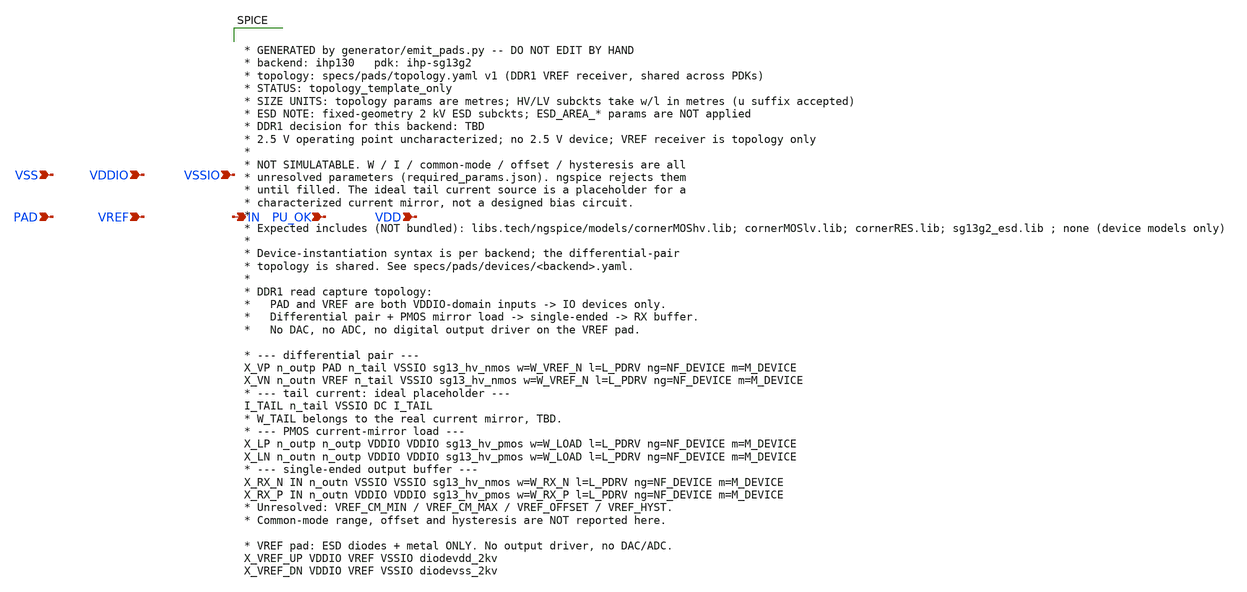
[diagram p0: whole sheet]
** sch_path: sch/pads/ihp130/vref_receiver.sch
**.subckt vref_receiver PAD VREF IN PU_OK VDD VSS VDDIO VSSIO
*.ipin PAD
*.ipin VREF
*.opin IN
*.ipin PU_OK
*.ipin VDD
*.ipin VSS
*.ipin VDDIO
*.ipin VSSIO
**** begin user architecture code


* GENERATED by generator/emit_pads.py -- DO NOT EDIT BY HAND
* backend: ihp130   pdk: ihp-sg13g2
* topology: specs/pads/topology.yaml v1 (DDR1 VREF receiver, shared across PDKs)
* STATUS: topology_template_only
* SIZE UNITS: topology params are metres; HV/LV subckts take w/l in metres (u suffix accepted)
* ESD NOTE: fixed-geometry 2 kV ESD subckts; ESD_AREA_* params are NOT applied
* DDR1 decision for this backend: TBD
* 2.5 V operating point uncharacterized; no 2.5 V device; VREF receiver is topology only
*
* NOT SIMULATABLE. W / I / common-mode / offset / hysteresis are all
* unresolved parameters (required_params.json). ngspice rejects them
* until filled. The ideal tail current source is a placeholder for a
* characterized current mirror, not a designed bias circuit.
*
* Expected includes (NOT bundled): libs.tech/ngspice/models/cornerMOShv.lib; cornerMOSlv.lib;
*+ cornerRES.lib; sg13g2_esd.lib ; none (device models only)
*
* Device-instantiation syntax is per backend; the differential-pair
* topology is shared. See specs/pads/devices/<backend>.yaml.
*
* DDR1 read capture topology:
*   PAD and VREF are both VDDIO-domain inputs -> IO devices only.
*   Differential pair + PMOS mirror load -> single-ended -> RX buffer.
*   No DAC, no ADC, no digital output driver on the VREF pad.

* --- differential pair ---
X_VP n_outp PAD n_tail VSSIO sg13_hv_nmos w=W_VREF_N l=L_PDRV ng=NF_DEVICE m=M_DEVICE
X_VN n_outn VREF n_tail VSSIO sg13_hv_nmos w=W_VREF_N l=L_PDRV ng=NF_DEVICE m=M_DEVICE
* --- tail current: ideal placeholder ---
I_TAIL n_tail VSSIO DC I_TAIL
* W_TAIL belongs to the real current mirror, TBD.
* --- PMOS current-mirror load ---
X_LP n_outp n_outp VDDIO VDDIO sg13_hv_pmos w=W_LOAD l=L_PDRV ng=NF_DEVICE m=M_DEVICE
X_LN n_outn n_outp VDDIO VDDIO sg13_hv_pmos w=W_LOAD l=L_PDRV ng=NF_DEVICE m=M_DEVICE
* --- single-ended output buffer ---
X_RX_N IN n_outn VSSIO VSSIO sg13_hv_nmos w=W_RX_N l=L_PDRV ng=NF_DEVICE m=M_DEVICE
X_RX_P IN n_outn VDDIO VDDIO sg13_hv_pmos w=W_RX_P l=L_PDRV ng=NF_DEVICE m=M_DEVICE
* Unresolved: VREF_CM_MIN / VREF_CM_MAX / VREF_OFFSET / VREF_HYST.
* Common-mode range, offset and hysteresis are NOT reported here.

* VREF pad: ESD diodes + metal ONLY. No output driver, no DAC/ADC.
X_VREF_UP VDDIO VREF VSSIO diodevdd_2kv
X_VREF_DN VDDIO VREF VSSIO diodevss_2kv


**** end user architecture code
**.ends
.end
